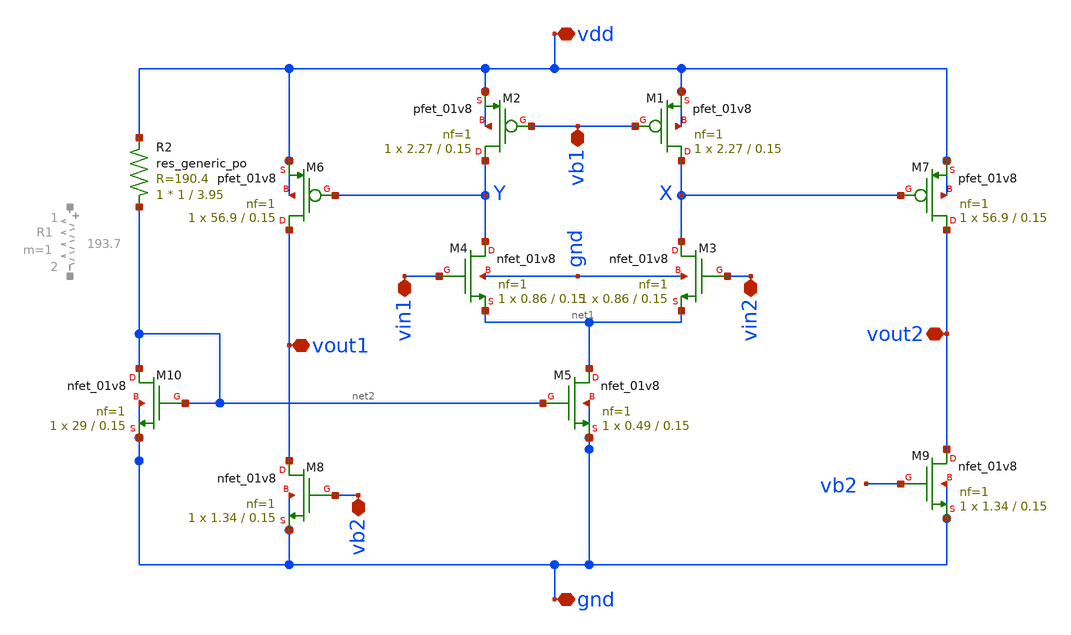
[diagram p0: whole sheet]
** sch_path: DIA3/opamp_final/opamp.sch
**.subckt opamp vdd gnd vout1 vout2 vin1 vin2 vb1 vb2
*.iopin vdd
*.iopin gnd
*.iopin vout1
*.iopin vout2
*.iopin vin1
*.iopin vin2
*.iopin vb1
*.iopin vb2
XM1 X vb1 vdd vdd sky130_fd_pr__pfet_01v8 L=0.15 W=2.27 nf=1 ad='int((nf+1)/2) * W/nf * 0.29' as='int((nf+2)/2) * W/nf * 0.29'
+ pd='2*int((nf+1)/2) * (W/nf + 0.29)' ps='2*int((nf+2)/2) * (W/nf + 0.29)' nrd='0.29 / W' nrs='0.29 / W'
+ sa=0 sb=0 sd=0 mult=1 m=1
XM2 Y vb1 vdd vdd sky130_fd_pr__pfet_01v8 L=0.15 W=2.27 nf=1 ad='int((nf+1)/2) * W/nf * 0.29' as='int((nf+2)/2) * W/nf * 0.29'
+ pd='2*int((nf+1)/2) * (W/nf + 0.29)' ps='2*int((nf+2)/2) * (W/nf + 0.29)' nrd='0.29 / W' nrs='0.29 / W'
+ sa=0 sb=0 sd=0 mult=1 m=1
XM3 X vin2 net1 gnd sky130_fd_pr__nfet_01v8 L=0.15 W=0.86 nf=1 ad='int((nf+1)/2) * W/nf * 0.29' as='int((nf+2)/2) * W/nf * 0.29'
+ pd='2*int((nf+1)/2) * (W/nf + 0.29)' ps='2*int((nf+2)/2) * (W/nf + 0.29)' nrd='0.29 / W' nrs='0.29 / W'
+ sa=0 sb=0 sd=0 mult=1 m=1
XM4 Y vin1 net1 gnd sky130_fd_pr__nfet_01v8 L=0.15 W=0.86 nf=1 ad='int((nf+1)/2) * W/nf * 0.29' as='int((nf+2)/2) * W/nf * 0.29'
+ pd='2*int((nf+1)/2) * (W/nf + 0.29)' ps='2*int((nf+2)/2) * (W/nf + 0.29)' nrd='0.29 / W' nrs='0.29 / W'
+ sa=0 sb=0 sd=0 mult=1 m=1
XM5 net1 net2 gnd gnd sky130_fd_pr__nfet_01v8 L=0.15 W=0.49 nf=1 ad='int((nf+1)/2) * W/nf * 0.29' as='int((nf+2)/2) * W/nf * 0.29'
+ pd='2*int((nf+1)/2) * (W/nf + 0.29)' ps='2*int((nf+2)/2) * (W/nf + 0.29)' nrd='0.29 / W' nrs='0.29 / W'
+ sa=0 sb=0 sd=0 mult=1 m=1
XM6 vout1 Y vdd vdd sky130_fd_pr__pfet_01v8 L=0.15 W=56.9 nf=1 ad='int((nf+1)/2) * W/nf * 0.29' as='int((nf+2)/2) * W/nf * 0.29'
+ pd='2*int((nf+1)/2) * (W/nf + 0.29)' ps='2*int((nf+2)/2) * (W/nf + 0.29)' nrd='0.29 / W' nrs='0.29 / W'
+ sa=0 sb=0 sd=0 mult=1 m=1
XM7 vout2 X vdd vdd sky130_fd_pr__pfet_01v8 L=0.15 W=56.9 nf=1 ad='int((nf+1)/2) * W/nf * 0.29' as='int((nf+2)/2) * W/nf * 0.29'
+ pd='2*int((nf+1)/2) * (W/nf + 0.29)' ps='2*int((nf+2)/2) * (W/nf + 0.29)' nrd='0.29 / W' nrs='0.29 / W'
+ sa=0 sb=0 sd=0 mult=1 m=1
XM8 vout1 vb2 gnd gnd sky130_fd_pr__nfet_01v8 L=0.15 W=1.34 nf=1 ad='int((nf+1)/2) * W/nf * 0.29' as='int((nf+2)/2) * W/nf * 0.29'
+ pd='2*int((nf+1)/2) * (W/nf + 0.29)' ps='2*int((nf+2)/2) * (W/nf + 0.29)' nrd='0.29 / W' nrs='0.29 / W'
+ sa=0 sb=0 sd=0 mult=1 m=1
XM9 vout2 vb2 gnd gnd sky130_fd_pr__nfet_01v8 L=0.15 W=1.34 nf=1 ad='int((nf+1)/2) * W/nf * 0.29' as='int((nf+2)/2) * W/nf * 0.29'
+ pd='2*int((nf+1)/2) * (W/nf + 0.29)' ps='2*int((nf+2)/2) * (W/nf + 0.29)' nrd='0.29 / W' nrs='0.29 / W'
+ sa=0 sb=0 sd=0 mult=1 m=1
XM10 net2 net2 gnd gnd sky130_fd_pr__nfet_01v8 L=0.15 W=29 nf=1 ad='int((nf+1)/2) * W/nf * 0.29' as='int((nf+2)/2) * W/nf * 0.29'
+ pd='2*int((nf+1)/2) * (W/nf + 0.29)' ps='2*int((nf+2)/2) * (W/nf + 0.29)' nrd='0.29 / W' nrs='0.29 / W'
+ sa=0 sb=0 sd=0 mult=1 m=1
XR2 net2 vdd sky130_fd_pr__res_generic_po W=1 L=3.95 m=1
**.ends
.end
